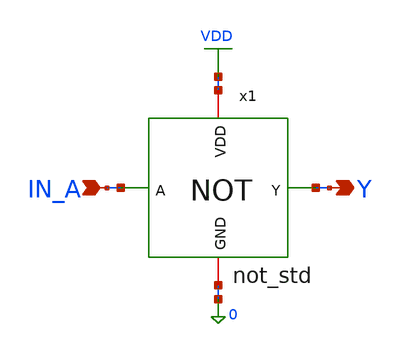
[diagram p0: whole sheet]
** sch_path: even_parity_generator/testbench/spice/tb_not.sch
**.subckt tb_not IN_A Y
*.ipin IN_A
*.opin Y
x1 VDD IN_A Y 0 not_std
**** begin user architecture code

.lib /foss/pdks/sky130A/libs.tech/ngspice/sky130.lib.spice tt

* --- VOLTAGE SOURCES ---
V_SUPPLY VDD 0 1.8
* IN_A period is 40ns to test all 2 states (0, 1)
V_A IN_A 0 pulse(0 1.8 1ns 100ps 100ps 19ns 40ns)

* --- SIMULATION COMMANDS ---
.tran 10p 100n
.dc V_A 0 1.8 0.01
.save all

.control
  run

  * --- VISUAL THEME ---
  set color0=white
  set color1=black
  set color2=red
  set color3=blue
  set color4=darkgreen
  set xbrushwidth=3

  * --- TIMING & POWER ANALYSIS ---
  setplot tran1

  * Universal Delay: measures time between first input crossing and first output crossing
  meas tran t_delay trig v(in_a) val=0.9 cross=1 targ v(y) val=0.9 cross=1

  * Power Analysis
  meas tran avg_i avg i(V_SUPPLY)
  let p_dyn = avg_i * 1.8 * -1

  meas tran leak_i find i(V_SUPPLY) at=99n
  let p_stat = leak_i * 1.8 * -1

  let pdp = p_dyn * t_delay

  * --- EXPORT CLEAN REPORT ---
  echo === NOT GATE REPORT === > report.txt
  echo Propagation Delay: >> report.txt
  print t_delay >> report.txt
  echo Dynamic Power: >> report.txt
  print p_dyn >> report.txt
  echo Static Power: >> report.txt
  print p_stat >> report.txt
  echo Power Delay Product: >> report.txt
  print pdp >> report.txt

  * --- 5. ADVANCED DATA PROCESSING & RAW EXPORT ---
  setplot tran1
  let inst_power = -i(V_SUPPLY) * 1.8
  let total_energy = integ(inst_power)

  write not_gate.raw

  * --- EXPORT PLOTS (SVG) ---
  set hcopydevtype=svg

  * Save DC Sweeps
  setplot dc1
  hardcopy dc_vtc.svg v(y) vs v(in_a) title 'DC: VTC'
  hardcopy dc_gain.svg v(y) vs v(in_a) deriv(v(y)) xl 0 1.8 yl -5 1.8 title 'DC: VTC and Noise Margins'

  * Save Transient Plots (Separated cleanly)
  setplot tran1
  hardcopy tran_inputs.svg v(in_a) title 'Transient: Logic Inputs'
  hardcopy tran_output.svg v(y) title 'Transient: Logic Output'
  hardcopy tran_current.svg -i(V_SUPPLY) title 'Transient: Total Supply Current'
  hardcopy tran_energy.svg total_energy title 'Transient: Cumulative Energy'
  hardcopy tran_leakage.svg -i(V_SUPPLY) yl 0 100n title 'Transient: Static Leakage Zoom'

  * --- SHOW PLOTS ON SCREEN ---
  * DC Plots
  setplot dc1
  plot v(y) vs v(in_a) title 'VTC'
  plot v(y) vs v(in_a) deriv(v(y)) xl 0 1.8 yl -5 1.8 title 'VTC and Noise Margins'

  * Transient Plots (Separated cleanly)
  setplot tran1
  plot v(in_a) title 'Logic Input (A)'
  plot v(y) title 'Logic Output (Y)'
  plot -i(V_SUPPLY) title 'Total Supply Current (Crowbar & Dynamic)'
  plot total_energy title 'Cumulative Energy Consumption'
  plot -i(V_SUPPLY) yl 0 100n title 'Static Leakage Current Zoom'
.endc

**** end user architecture code
**.ends

* expanding   symbol:  schematic/not_std.sym # of pins=4
** sym_path: parity_ceker/schematic/not_std.sym
** sch_path: parity_ceker/schematic/not_std.sch
.subckt not_std VDD A Y GND
*.ipin A
*.opin Y
*.iopin VDD
*.iopin GND
XM1 Y A VDD VDD sky130_fd_pr__pfet_01v8 L=0.15 W=2 nf=1 ad='int((1 + 1)/2) * 2 / 1 * 0.29' as='int((1 + 2)/2) * 2 / 1 * 0.29'
+ pd='2*int((1 + 1)/2) * (2 / 1 + 0.29)' ps='2*int((1 + 2)/2) * (2 / 1 + 0.29)' nrd='0.29 / 2 ' nrs='0.29 / 2 '
+ sa=0 sb=0 sd=0 mult=1 m=1
XM2 Y A GND GND sky130_fd_pr__nfet_01v8 L=0.15 W=1 nf=1 ad='int((1 + 1)/2) * 1 / 1 * 0.29' as='int((1 + 2)/2) * 1 / 1 * 0.29'
+ pd='2*int((1 + 1)/2) * (1 / 1 + 0.29)' ps='2*int((1 + 2)/2) * (1 / 1 + 0.29)' nrd='0.29 / 1 ' nrs='0.29 / 1 '
+ sa=0 sb=0 sd=0 mult=1 m=1
.ends

.GLOBAL VDD
.end
